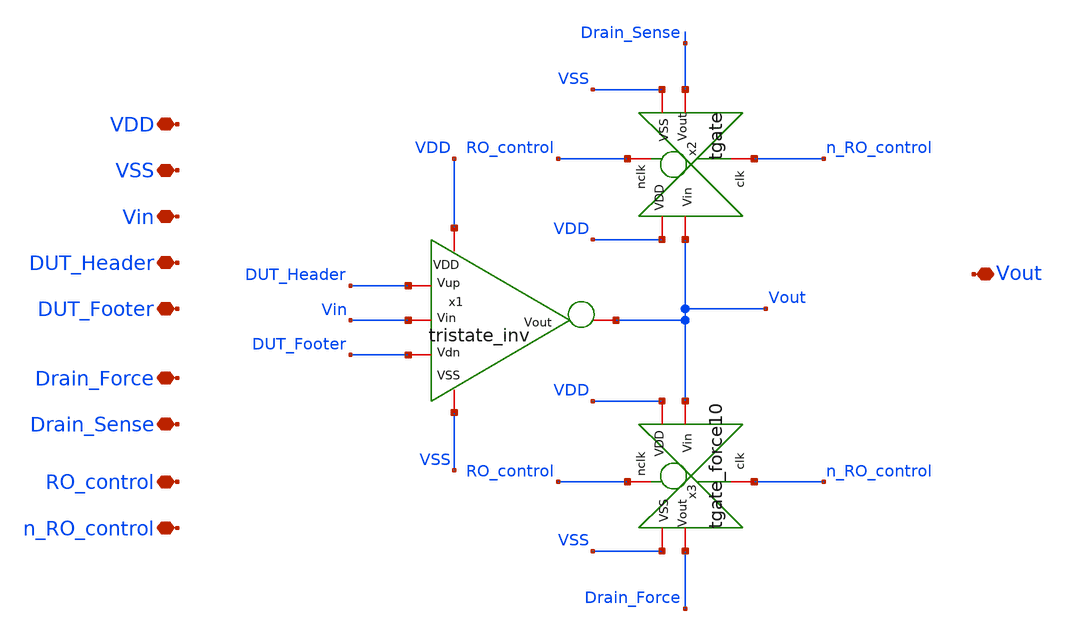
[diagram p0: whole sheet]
** sch_path: unic_cass_wrapper_user_project/ROs_reliability/rovcel1_10.sch
**.subckt rovcel1_10 VDD VSS Vin DUT_Header DUT_Footer Drain_Force Vout Drain_Sense RO_control
*+ n_RO_control
*.iopin VDD
*.iopin VSS
*.iopin Vin
*.iopin DUT_Header
*.iopin DUT_Footer
*.iopin Drain_Force
*.iopin Vout
*.iopin Drain_Sense
*.iopin RO_control
*.iopin n_RO_control
x1 VDD VSS Vin DUT_Header DUT_Footer Vout tristate_inv
x2 RO_control VDD Vout Drain_Sense VSS n_RO_control tgate
x3 RO_control VDD Vout Drain_Force VSS n_RO_control tgate_force10
**.ends

* expanding   symbol:  tristate_inv.sym # of pins=6
** sym_path: tristate_inv.sym
** sch_path: tristate_inv.sch
.subckt tristate_inv VDD VSS Vin Vup Vdn Vout
*.iopin VDD
*.iopin VSS
*.iopin Vin
*.iopin Vout
*.iopin Vup
*.iopin Vdn
XM5 Vout Vin net1 VDD sg13_lv_pmos w=3.4u l=0.45u ng=1 m=4 mm_ok=1
XM2 net2 Vin Vout VSS sg13_lv_nmos w=1.3u l=0.45u ng=1 m=4 mm_ok=1
XM1 net1 Vup VDD VDD sg13_lv_pmos w=3.4u l=0.45u ng=1 m=12 mm_ok=1
XM3 VSS Vdn net2 VSS sg13_lv_nmos w=1.3u l=0.45u ng=1 m=12 mm_ok=1
.ends


* expanding   symbol:  tgate.sym # of pins=6
** sym_path: tgate.sym
** sch_path: tgate.sch
.subckt tgate nclk VDD Vin Vout VSS clk
*.iopin nclk
*.iopin clk
*.iopin VDD
*.iopin VSS
*.iopin Vout
*.iopin Vin
XM3 Vout nclk Vin VDD sg13_lv_pmos w=3.4u l=0.45u ng=1 m=1 mm_ok=1
XM1 Vout clk Vin VSS sg13_lv_nmos w=1.3u l=0.45u ng=1 m=1 mm_ok=1
.ends


* expanding   symbol:  tgate_force10.sym # of pins=6
** sym_path: tgate_force10.sym
** sch_path: tgate_force10.sch
.subckt tgate_force10 nclk VDD Vin Vout VSS clk
*.iopin nclk
*.iopin clk
*.iopin VDD
*.iopin VSS
*.iopin Vout
*.iopin Vin
XM1 Vout nclk Vin VDD sg13_lv_pmos w=3.4u l=0.45u ng=1 m=12 mm_ok=1
XM3 Vout clk Vin VSS sg13_lv_nmos w=1.3u l=0.45u ng=1 m=12 mm_ok=1
.ends

.end
